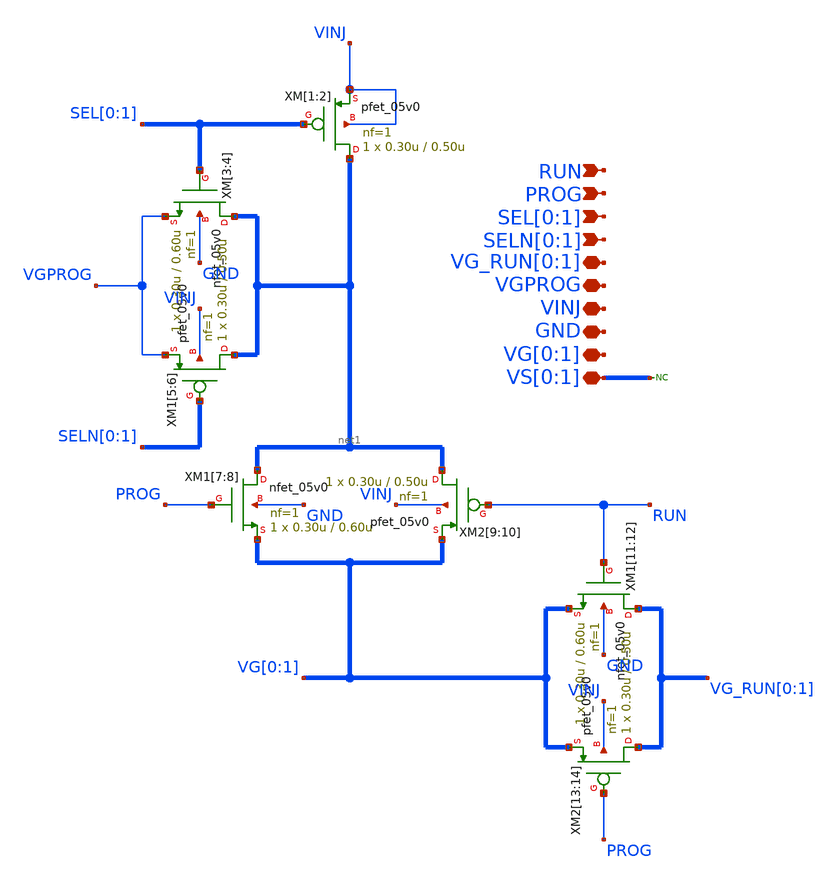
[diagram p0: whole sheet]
** sch_path: 4_Schematics/SWC_Gate.sch
**.subckt SWC_Gate RUN PROG SEL[0],SEL[1] SELN[0],SELN[1] VG_RUN[0],VG_RUN[1] VGPROG VINJ GND
*+ VG[0],VG[1] VS[0],VS[1]
*.ipin RUN
*.ipin PROG
*.ipin SEL[0],SEL[1]
*.ipin SELN[0],SELN[1]
*.iopin VG_RUN[0],VG_RUN[1]
*.iopin VGPROG
*.iopin VINJ
*.iopin GND
*.iopin VG[0],VG[1]
*.iopin VS[0],VS[1]
XM[1] net1[1] SEL[0] VINJ VINJ pfet_05v0 L=0.50u W=0.30u nf=1 ad='int((nf+1)/2) * W/nf * 0.18u' as='int((nf+2)/2) * W/nf * 0.18u'
+ pd='2*int((nf+1)/2) * (W/nf + 0.18u)' ps='2*int((nf+2)/2) * (W/nf + 0.18u)' nrd='0.18u / W' nrs='0.18u / W'
+ sa=0 sb=0 sd=0 m=1
XM[2] net1[0] SEL[1] VINJ VINJ pfet_05v0 L=0.50u W=0.30u nf=1 ad='int((nf+1)/2) * W/nf * 0.18u' as='int((nf+2)/2) * W/nf * 0.18u'
+ pd='2*int((nf+1)/2) * (W/nf + 0.18u)' ps='2*int((nf+2)/2) * (W/nf + 0.18u)' nrd='0.18u / W' nrs='0.18u / W'
+ sa=0 sb=0 sd=0 m=1
XM[3] net1[1] SEL[0] VGPROG GND nfet_05v0 L=0.60u W=0.30u nf=1 ad='int((nf+1)/2) * W/nf * 0.18u' as='int((nf+2)/2) * W/nf * 0.18u'
+ pd='2*int((nf+1)/2) * (W/nf + 0.18u)' ps='2*int((nf+2)/2) * (W/nf + 0.18u)' nrd='0.18u / W' nrs='0.18u / W'
+ sa=0 sb=0 sd=0 m=1
XM[4] net1[0] SEL[1] VGPROG GND nfet_05v0 L=0.60u W=0.30u nf=1 ad='int((nf+1)/2) * W/nf * 0.18u' as='int((nf+2)/2) * W/nf * 0.18u'
+ pd='2*int((nf+1)/2) * (W/nf + 0.18u)' ps='2*int((nf+2)/2) * (W/nf + 0.18u)' nrd='0.18u / W' nrs='0.18u / W'
+ sa=0 sb=0 sd=0 m=1
XM1[5] net1[1] SELN[0] VGPROG VINJ pfet_05v0 L=0.50u W=0.30u nf=1 ad='int((nf+1)/2) * W/nf * 0.18u' as='int((nf+2)/2) * W/nf * 0.18u'
+ pd='2*int((nf+1)/2) * (W/nf + 0.18u)' ps='2*int((nf+2)/2) * (W/nf + 0.18u)' nrd='0.18u / W' nrs='0.18u / W'
+ sa=0 sb=0 sd=0 m=1
XM1[6] net1[0] SELN[1] VGPROG VINJ pfet_05v0 L=0.50u W=0.30u nf=1 ad='int((nf+1)/2) * W/nf * 0.18u' as='int((nf+2)/2) * W/nf * 0.18u'
+ pd='2*int((nf+1)/2) * (W/nf + 0.18u)' ps='2*int((nf+2)/2) * (W/nf + 0.18u)' nrd='0.18u / W' nrs='0.18u / W'
+ sa=0 sb=0 sd=0 m=1
XM1[7] net1[1] PROG VG[0] GND nfet_05v0 L=0.60u W=0.30u nf=1 ad='int((nf+1)/2) * W/nf * 0.18u' as='int((nf+2)/2) * W/nf * 0.18u'
+ pd='2*int((nf+1)/2) * (W/nf + 0.18u)' ps='2*int((nf+2)/2) * (W/nf + 0.18u)' nrd='0.18u / W' nrs='0.18u / W'
+ sa=0 sb=0 sd=0 m=1
XM1[8] net1[0] PROG VG[1] GND nfet_05v0 L=0.60u W=0.30u nf=1 ad='int((nf+1)/2) * W/nf * 0.18u' as='int((nf+2)/2) * W/nf * 0.18u'
+ pd='2*int((nf+1)/2) * (W/nf + 0.18u)' ps='2*int((nf+2)/2) * (W/nf + 0.18u)' nrd='0.18u / W' nrs='0.18u / W'
+ sa=0 sb=0 sd=0 m=1
XM2[9] net1[1] RUN VG[0] VINJ pfet_05v0 L=0.50u W=0.30u nf=1 ad='int((nf+1)/2) * W/nf * 0.18u' as='int((nf+2)/2) * W/nf * 0.18u'
+ pd='2*int((nf+1)/2) * (W/nf + 0.18u)' ps='2*int((nf+2)/2) * (W/nf + 0.18u)' nrd='0.18u / W' nrs='0.18u / W'
+ sa=0 sb=0 sd=0 m=1
XM2[10] net1[0] RUN VG[1] VINJ pfet_05v0 L=0.50u W=0.30u nf=1 ad='int((nf+1)/2) * W/nf * 0.18u' as='int((nf+2)/2) * W/nf * 0.18u'
+ pd='2*int((nf+1)/2) * (W/nf + 0.18u)' ps='2*int((nf+2)/2) * (W/nf + 0.18u)' nrd='0.18u / W' nrs='0.18u / W'
+ sa=0 sb=0 sd=0 m=1
XM1[11] VG_RUN[0] RUN VG[0] GND nfet_05v0 L=0.60u W=0.30u nf=1 ad='int((nf+1)/2) * W/nf * 0.18u' as='int((nf+2)/2) * W/nf * 0.18u'
+ pd='2*int((nf+1)/2) * (W/nf + 0.18u)' ps='2*int((nf+2)/2) * (W/nf + 0.18u)' nrd='0.18u / W' nrs='0.18u / W'
+ sa=0 sb=0 sd=0 m=1
XM1[12] VG_RUN[1] RUN VG[1] GND nfet_05v0 L=0.60u W=0.30u nf=1 ad='int((nf+1)/2) * W/nf * 0.18u' as='int((nf+2)/2) * W/nf * 0.18u'
+ pd='2*int((nf+1)/2) * (W/nf + 0.18u)' ps='2*int((nf+2)/2) * (W/nf + 0.18u)' nrd='0.18u / W' nrs='0.18u / W'
+ sa=0 sb=0 sd=0 m=1
XM2[13] VG_RUN[0] PROG VG[0] VINJ pfet_05v0 L=0.50u W=0.30u nf=1 ad='int((nf+1)/2) * W/nf * 0.18u' as='int((nf+2)/2) * W/nf * 0.18u'
+ pd='2*int((nf+1)/2) * (W/nf + 0.18u)' ps='2*int((nf+2)/2) * (W/nf + 0.18u)' nrd='0.18u / W' nrs='0.18u / W'
+ sa=0 sb=0 sd=0 m=1
XM2[14] VG_RUN[1] PROG VG[1] VINJ pfet_05v0 L=0.50u W=0.30u nf=1 ad='int((nf+1)/2) * W/nf * 0.18u' as='int((nf+2)/2) * W/nf * 0.18u'
+ pd='2*int((nf+1)/2) * (W/nf + 0.18u)' ps='2*int((nf+2)/2) * (W/nf + 0.18u)' nrd='0.18u / W' nrs='0.18u / W'
+ sa=0 sb=0 sd=0 m=1
* noconn VS[0:1]
**.ends
.end
